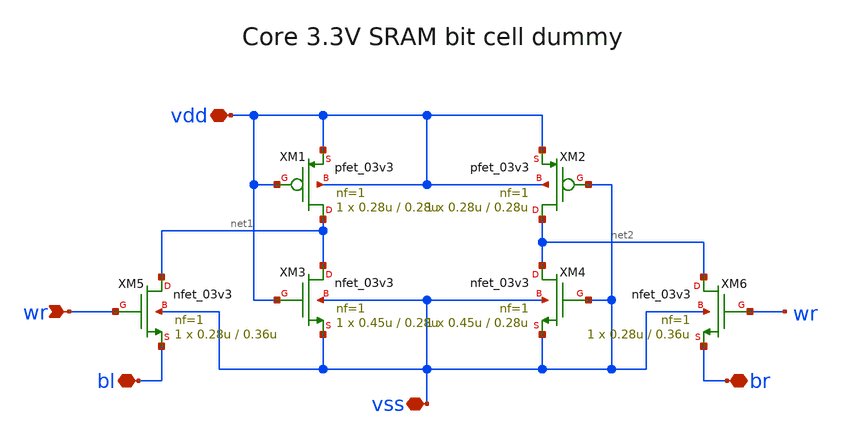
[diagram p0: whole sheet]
** sch_path: cells/gf180mcu_ocd_ip_sram__sram1024x8m8wm1/xschem/x018SRAM_cell1_dummy_R_3v1024x8m81.sch
**.subckt x018SRAM_cell1_dummy_R_3v1024x8m81 vdd vss wr bl br
*.iopin vdd
*.iopin vss
*.ipin wr
*.iopin bl
*.iopin br
XM1 net1 vdd vdd vdd pfet_03v3 L=0.28u W=0.28u nf=1 ad='int((nf+1)/2) * W/nf * 0.18u' as='int((nf+2)/2) * W/nf * 0.18u'
+ pd='2*int((nf+1)/2) * (W/nf + 0.18u)' ps='2*int((nf+2)/2) * (W/nf + 0.18u)' nrd='0.18u / W' nrs='0.18u / W'
+ sa=0 sb=0 sd=0 m=1
XM2 net2 vss vdd vdd pfet_03v3 L=0.28u W=0.28u nf=1 ad='int((nf+1)/2) * W/nf * 0.18u' as='int((nf+2)/2) * W/nf * 0.18u'
+ pd='2*int((nf+1)/2) * (W/nf + 0.18u)' ps='2*int((nf+2)/2) * (W/nf + 0.18u)' nrd='0.18u / W' nrs='0.18u / W'
+ sa=0 sb=0 sd=0 m=1
XM3 net1 vdd vss vss nfet_03v3 L=0.28u W=0.45u nf=1 ad='int((nf+1)/2) * W/nf * 0.18u' as='int((nf+2)/2) * W/nf * 0.18u'
+ pd='2*int((nf+1)/2) * (W/nf + 0.18u)' ps='2*int((nf+2)/2) * (W/nf + 0.18u)' nrd='0.18u / W' nrs='0.18u / W'
+ sa=0 sb=0 sd=0 m=1
XM4 net2 vss vss vss nfet_03v3 L=0.28u W=0.45u nf=1 ad='int((nf+1)/2) * W/nf * 0.18u' as='int((nf+2)/2) * W/nf * 0.18u'
+ pd='2*int((nf+1)/2) * (W/nf + 0.18u)' ps='2*int((nf+2)/2) * (W/nf + 0.18u)' nrd='0.18u / W' nrs='0.18u / W'
+ sa=0 sb=0 sd=0 m=1
XM5 net1 wr bl vss nfet_03v3 L=0.36u W=0.28u nf=1 ad='int((nf+1)/2) * W/nf * 0.18u' as='int((nf+2)/2) * W/nf * 0.18u'
+ pd='2*int((nf+1)/2) * (W/nf + 0.18u)' ps='2*int((nf+2)/2) * (W/nf + 0.18u)' nrd='0.18u / W' nrs='0.18u / W'
+ sa=0 sb=0 sd=0 m=1
XM6 net2 wr br vss nfet_03v3 L=0.36u W=0.28u nf=1 ad='int((nf+1)/2) * W/nf * 0.18u' as='int((nf+2)/2) * W/nf * 0.18u'
+ pd='2*int((nf+1)/2) * (W/nf + 0.18u)' ps='2*int((nf+2)/2) * (W/nf + 0.18u)' nrd='0.18u / W' nrs='0.18u / W'
+ sa=0 sb=0 sd=0 m=1
**.ends
.end
